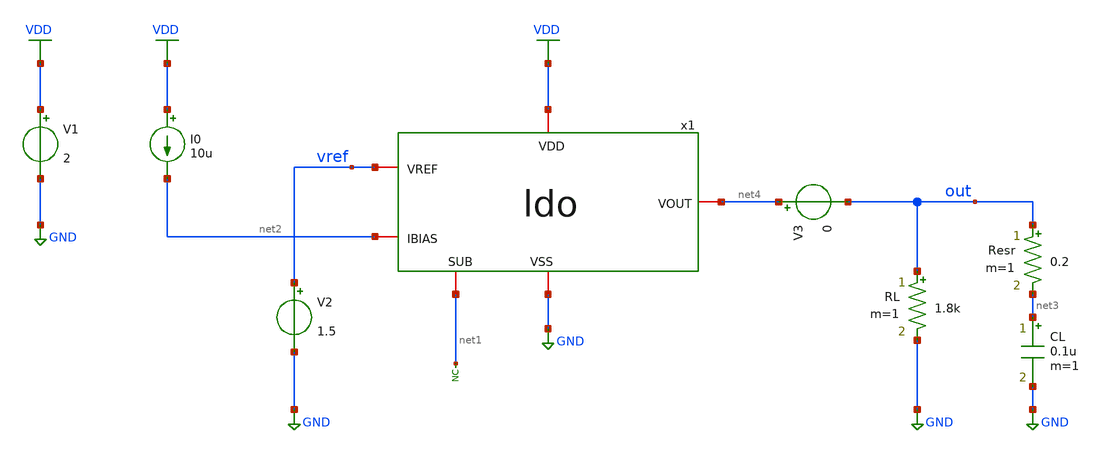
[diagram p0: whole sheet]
** sch_path: designs/libs/tb_ldo/tb_ldo/tb_ldo/tb_ldo_op/tb_ldo_op.sch
**.subckt tb_ldo_op
* noconn #net1
RL out GND 1.8k m=1
V1 VDD GND 2
V2 vref GND 1.5
I0 VDD net2 10u
CL net3 GND 0.1u m=1
Resr out net3 0.2 m=1
x1 VDD vref net4 net2 net1 GND ldo
V3 net4 out 0
**** begin user architecture code

.include $::180MCU_MODELS/design.ngspice
.lib $::180MCU_MODELS/sm141064.ngspice typical
.lib $::180MCU_MODELS/sm141064.ngspice cap_mim
.lib $::180MCU_MODELS/sm141064.ngspice moscap_typical
.lib $::180MCU_MODELS/sm141064.ngspice mimcap_typical
.lib $::180MCU_MODELS/sm141064.ngspice res_typical
* .lib $::180MCU_MODELS/sm141064.ngspice res_statistical
* ngspice commands




.control
save all

** Simulations
op

** Measurements
show all
let Iload = i(V3)
let Itot = -1*i(V1)
let Iq = Itot-Iload
let Ptot = v(vdd)*Itot
let Pload = Iload*v(out)
let Pldo = Ptot-Pload
let eff = (Pload/Ptot)*100
print Itot
print Iload
print Iq
print Ptot
print Pload
print Pldo
print eff

write tb_ldo_op.raw
.endc
* ngspice commands



**** end user architecture code
**.ends
.GLOBAL GND
.GLOBAL VDD
.end
